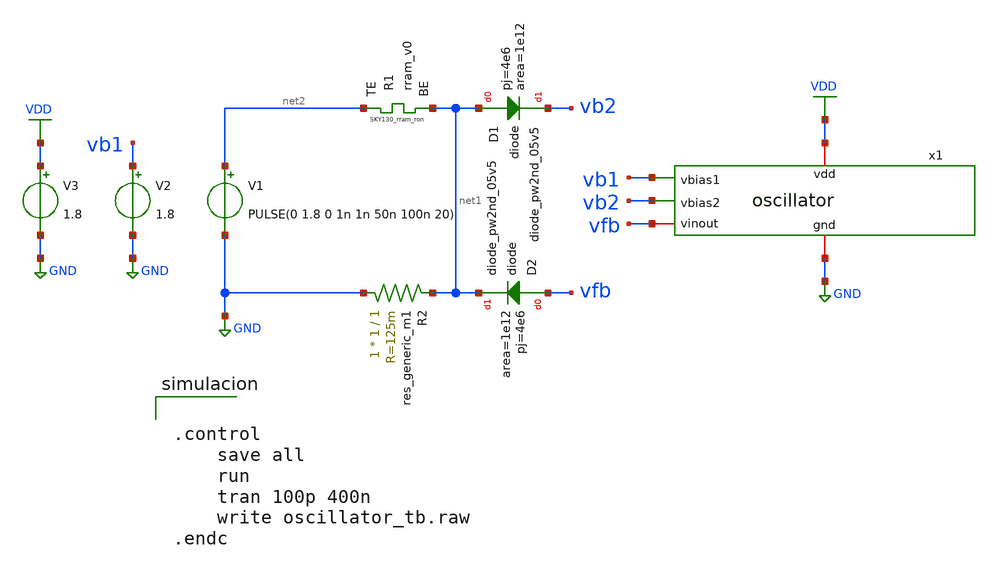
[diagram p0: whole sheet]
** sch_path: oscillator/oscillator_rram_tb.sch
**.subckt oscillator_rram_tb
x1 VDD vb1 vfb vb2 GND oscillator
V1 net2 GND PULSE(0 1.8 0 1n 1n 50n 100n 20)
.save i(v1)
XD1 net1 vb2 sky130_fd_pr__diode_pw2nd_05v5 area=1e12 pj=4e6
XD2 vfb net1 sky130_fd_pr__diode_pw2nd_05v5 area=1e12 pj=4e6
R2 GND net1 sky130_fd_pr__res_generic_m1 W=1 L=1 m=1
V2 vb1 GND 1.8
.save i(v2)
V3 VDD GND 1.8
.save i(v3)
XR1 net2 net1 rram_v0
**** begin user architecture code

** opencircuitdesign pdks install
.lib $::SKYWATER_MODELS/sky130.lib.spice tt




.control
	save all
	run
	tran 100p 400n
	write oscillator_tb.raw
.endc


**** end user architecture code
**.ends
.GLOBAL VDD
.GLOBAL GND
.end
